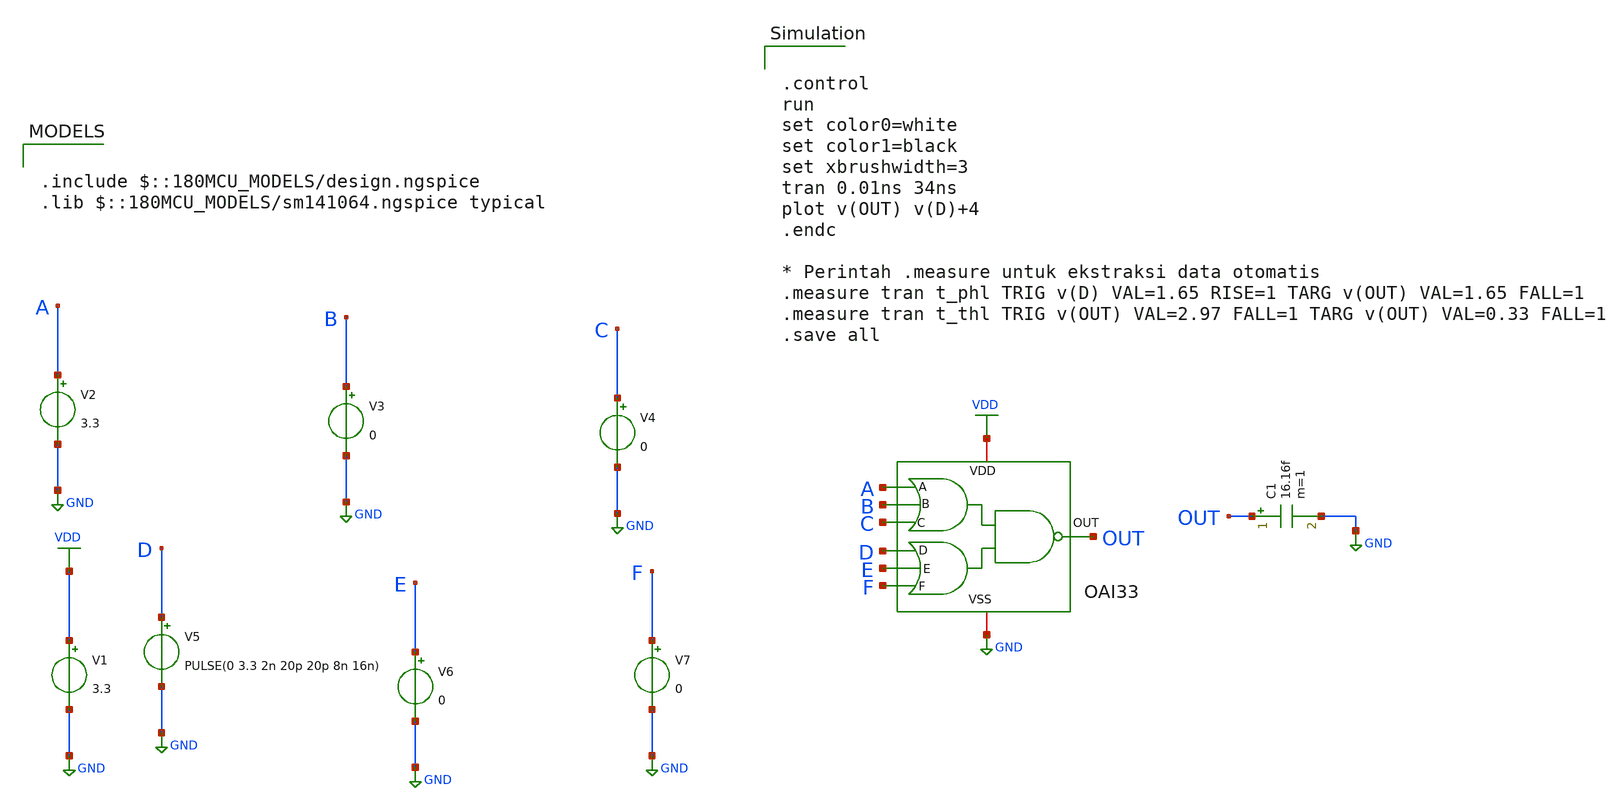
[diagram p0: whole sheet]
** sch_path: designs/OAI33/xschem/OAI33_tb.sch
**.subckt OAI33_tb
V1 VDD GND 3.3
V2 A GND 3.3
V3 B GND 0
V4 C GND 0
V5 D GND PULSE(0 3.3 2n 20p 20p 8n 16n)
V6 E GND 0
V7 F GND 0
C1 OUT GND 16.16f m=1
x1 VDD GND A D B E F C OUT OAI33
**** begin user architecture code

.include $::180MCU_MODELS/design.ngspice
.lib $::180MCU_MODELS/sm141064.ngspice typical



.control
run
set color0=white
set color1=black
set xbrushwidth=3
tran 0.01ns 34ns
plot v(OUT) v(D)+4
.endc

* Perintah .measure untuk ekstraksi data otomatis
.measure tran t_phl TRIG v(D) VAL=1.65 RISE=1 TARG v(OUT) VAL=1.65 FALL=1
.measure tran t_thl TRIG v(OUT) VAL=2.97 FALL=1 TARG v(OUT) VAL=0.33 FALL=1
.save all

**** end user architecture code
**.ends
.GLOBAL VDD
.GLOBAL GND
.end
